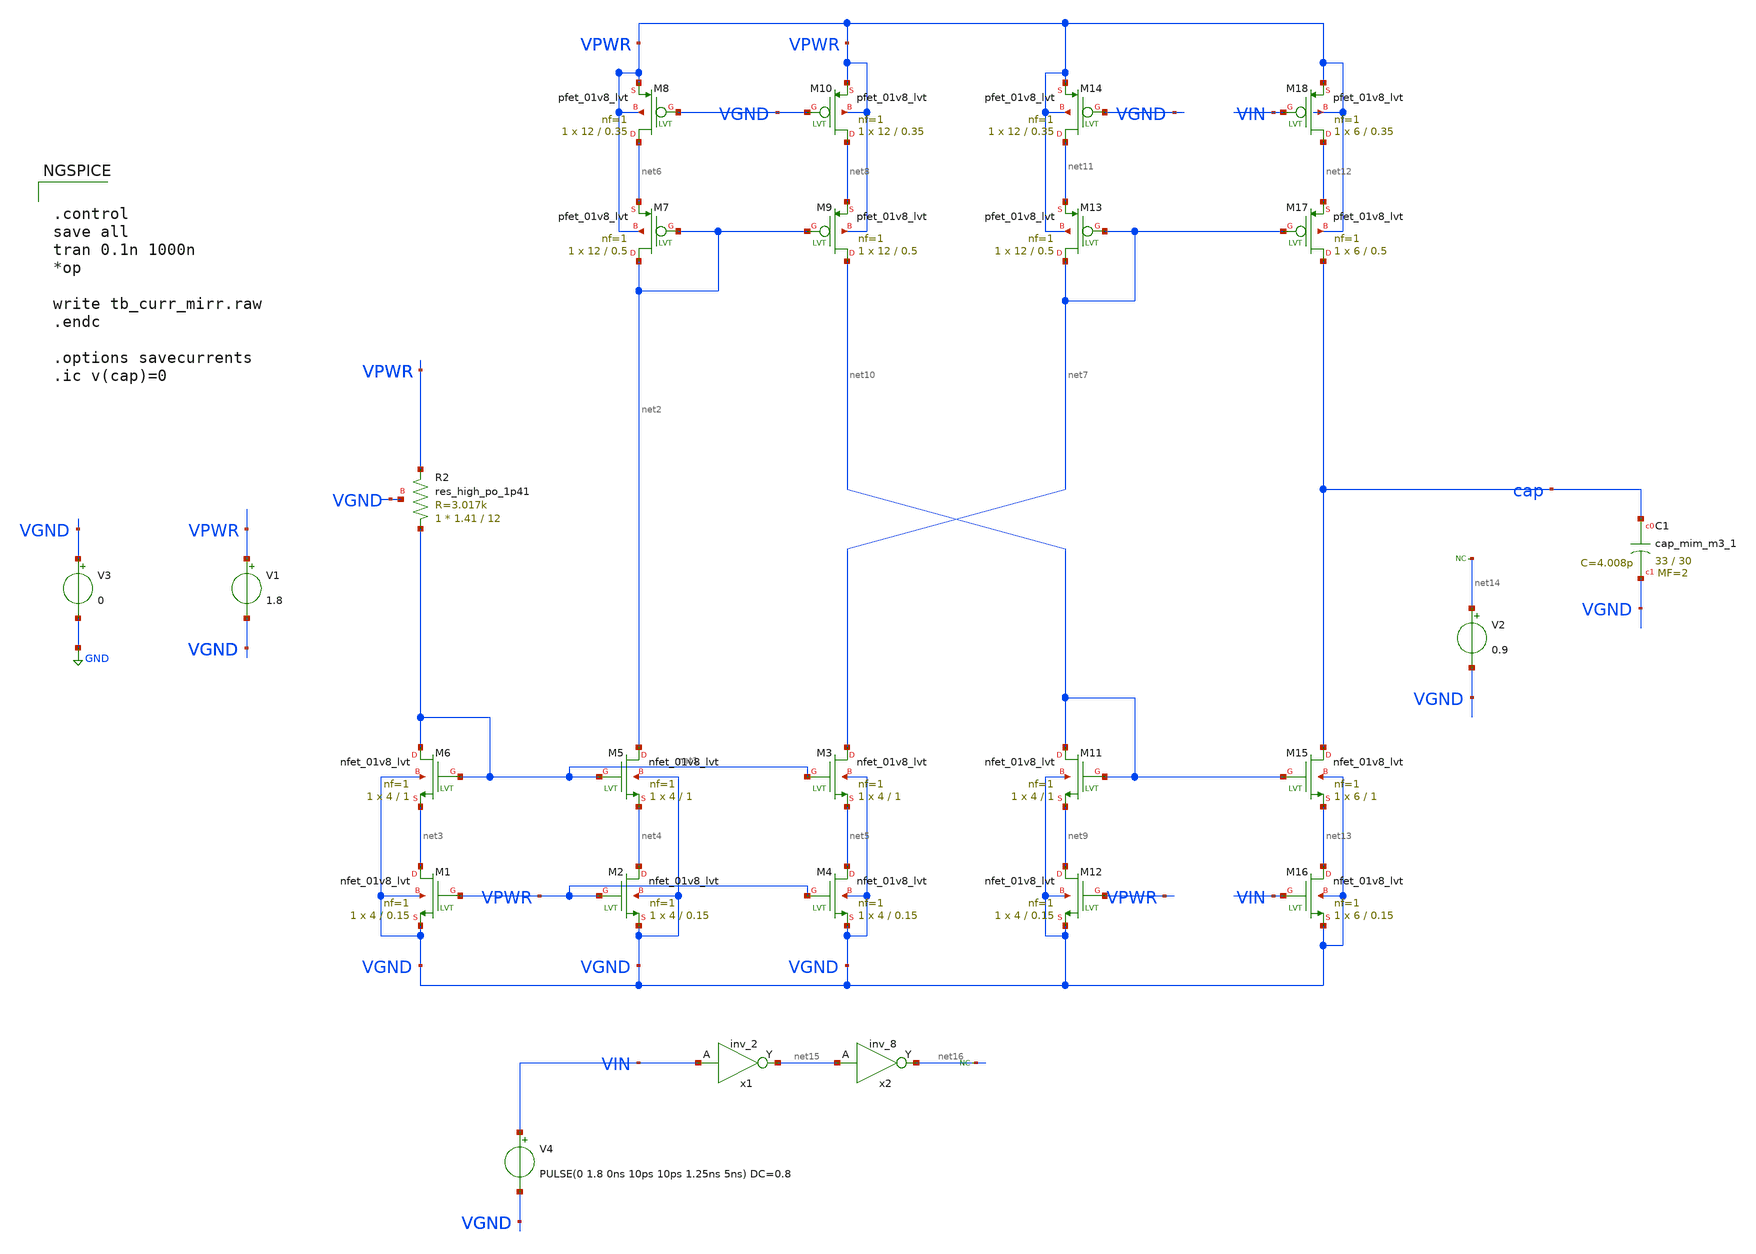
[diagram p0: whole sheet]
** sch_path: design/tb_curr_mirr.sch
**.subckt tb_curr_mirr
V1 VPWR VGND 1.8
V3 VGND GND 0
XM5 net2 net1 net4 VGND sky130_fd_pr__nfet_01v8_lvt L=1 W=4 nf=1 ad='int((nf+1)/2) * W/nf * 0.29' as='int((nf+2)/2) * W/nf * 0.29'
+ pd='2*int((nf+1)/2) * (W/nf + 0.29)' ps='2*int((nf+2)/2) * (W/nf + 0.29)' nrd='0.29 / W' nrs='0.29 / W'
+ sa=0 sb=0 sd=0 mult=1 m=1
XM6 net1 net1 net3 VGND sky130_fd_pr__nfet_01v8_lvt L=1 W=4 nf=1 ad='int((nf+1)/2) * W/nf * 0.29' as='int((nf+2)/2) * W/nf * 0.29'
+ pd='2*int((nf+1)/2) * (W/nf + 0.29)' ps='2*int((nf+2)/2) * (W/nf + 0.29)' nrd='0.29 / W' nrs='0.29 / W'
+ sa=0 sb=0 sd=0 mult=1 m=1
XM1 net3 VPWR VGND VGND sky130_fd_pr__nfet_01v8_lvt L=0.15 W=4 nf=1 ad='int((nf+1)/2) * W/nf * 0.29'
+ as='int((nf+2)/2) * W/nf * 0.29' pd='2*int((nf+1)/2) * (W/nf + 0.29)' ps='2*int((nf+2)/2) * (W/nf + 0.29)'
+ nrd='0.29 / W' nrs='0.29 / W' sa=0 sb=0 sd=0 mult=1 m=1
XM2 net4 VPWR VGND VGND sky130_fd_pr__nfet_01v8_lvt L=0.15 W=4 nf=1 ad='int((nf+1)/2) * W/nf * 0.29'
+ as='int((nf+2)/2) * W/nf * 0.29' pd='2*int((nf+1)/2) * (W/nf + 0.29)' ps='2*int((nf+2)/2) * (W/nf + 0.29)'
+ nrd='0.29 / W' nrs='0.29 / W' sa=0 sb=0 sd=0 mult=1 m=1
XM3 net7 net1 net5 VGND sky130_fd_pr__nfet_01v8_lvt L=1 W=4 nf=1 ad='int((nf+1)/2) * W/nf * 0.29' as='int((nf+2)/2) * W/nf * 0.29'
+ pd='2*int((nf+1)/2) * (W/nf + 0.29)' ps='2*int((nf+2)/2) * (W/nf + 0.29)' nrd='0.29 / W' nrs='0.29 / W'
+ sa=0 sb=0 sd=0 mult=1 m=1
XM4 net5 VPWR VGND VGND sky130_fd_pr__nfet_01v8_lvt L=0.15 W=4 nf=1 ad='int((nf+1)/2) * W/nf * 0.29'
+ as='int((nf+2)/2) * W/nf * 0.29' pd='2*int((nf+1)/2) * (W/nf + 0.29)' ps='2*int((nf+2)/2) * (W/nf + 0.29)'
+ nrd='0.29 / W' nrs='0.29 / W' sa=0 sb=0 sd=0 mult=1 m=1
XM7 net2 net2 net6 VPWR sky130_fd_pr__pfet_01v8_lvt L=0.5 W=12 nf=1 ad='int((nf+1)/2) * W/nf * 0.29'
+ as='int((nf+2)/2) * W/nf * 0.29' pd='2*int((nf+1)/2) * (W/nf + 0.29)' ps='2*int((nf+2)/2) * (W/nf + 0.29)'
+ nrd='0.29 / W' nrs='0.29 / W' sa=0 sb=0 sd=0 mult=1 m=1
XM8 net6 VGND VPWR VPWR sky130_fd_pr__pfet_01v8_lvt L=0.35 W=12 nf=1 ad='int((nf+1)/2) * W/nf * 0.29'
+ as='int((nf+2)/2) * W/nf * 0.29' pd='2*int((nf+1)/2) * (W/nf + 0.29)' ps='2*int((nf+2)/2) * (W/nf + 0.29)'
+ nrd='0.29 / W' nrs='0.29 / W' sa=0 sb=0 sd=0 mult=1 m=1
XM9 net10 net2 net8 VPWR sky130_fd_pr__pfet_01v8_lvt L=0.5 W=12 nf=1 ad='int((nf+1)/2) * W/nf * 0.29'
+ as='int((nf+2)/2) * W/nf * 0.29' pd='2*int((nf+1)/2) * (W/nf + 0.29)' ps='2*int((nf+2)/2) * (W/nf + 0.29)'
+ nrd='0.29 / W' nrs='0.29 / W' sa=0 sb=0 sd=0 mult=1 m=1
XM10 net8 VGND VPWR VPWR sky130_fd_pr__pfet_01v8_lvt L=0.35 W=12 nf=1 ad='int((nf+1)/2) * W/nf * 0.29'
+ as='int((nf+2)/2) * W/nf * 0.29' pd='2*int((nf+1)/2) * (W/nf + 0.29)' ps='2*int((nf+2)/2) * (W/nf + 0.29)'
+ nrd='0.29 / W' nrs='0.29 / W' sa=0 sb=0 sd=0 mult=1 m=1
XM11 net10 net10 net9 VGND sky130_fd_pr__nfet_01v8_lvt L=1 W=4 nf=1 ad='int((nf+1)/2) * W/nf * 0.29'
+ as='int((nf+2)/2) * W/nf * 0.29' pd='2*int((nf+1)/2) * (W/nf + 0.29)' ps='2*int((nf+2)/2) * (W/nf + 0.29)'
+ nrd='0.29 / W' nrs='0.29 / W' sa=0 sb=0 sd=0 mult=1 m=1
XM12 net9 VPWR VGND VGND sky130_fd_pr__nfet_01v8_lvt L=0.15 W=4 nf=1 ad='int((nf+1)/2) * W/nf * 0.29'
+ as='int((nf+2)/2) * W/nf * 0.29' pd='2*int((nf+1)/2) * (W/nf + 0.29)' ps='2*int((nf+2)/2) * (W/nf + 0.29)'
+ nrd='0.29 / W' nrs='0.29 / W' sa=0 sb=0 sd=0 mult=1 m=1
XM13 net7 net7 net11 VPWR sky130_fd_pr__pfet_01v8_lvt L=0.5 W=12 nf=1 ad='int((nf+1)/2) * W/nf * 0.29'
+ as='int((nf+2)/2) * W/nf * 0.29' pd='2*int((nf+1)/2) * (W/nf + 0.29)' ps='2*int((nf+2)/2) * (W/nf + 0.29)'
+ nrd='0.29 / W' nrs='0.29 / W' sa=0 sb=0 sd=0 mult=1 m=1
XM14 net11 VGND VPWR VPWR sky130_fd_pr__pfet_01v8_lvt L=0.35 W=12 nf=1 ad='int((nf+1)/2) * W/nf * 0.29'
+ as='int((nf+2)/2) * W/nf * 0.29' pd='2*int((nf+1)/2) * (W/nf + 0.29)' ps='2*int((nf+2)/2) * (W/nf + 0.29)'
+ nrd='0.29 / W' nrs='0.29 / W' sa=0 sb=0 sd=0 mult=1 m=1
XM15 cap net10 net13 VGND sky130_fd_pr__nfet_01v8_lvt L=1 W=6 nf=1 ad='int((nf+1)/2) * W/nf * 0.29' as='int((nf+2)/2) * W/nf * 0.29'
+ pd='2*int((nf+1)/2) * (W/nf + 0.29)' ps='2*int((nf+2)/2) * (W/nf + 0.29)' nrd='0.29 / W' nrs='0.29 / W'
+ sa=0 sb=0 sd=0 mult=1 m=1
XM17 cap net7 net12 VPWR sky130_fd_pr__pfet_01v8_lvt L=0.5 W=6 nf=1 ad='int((nf+1)/2) * W/nf * 0.29'
+ as='int((nf+2)/2) * W/nf * 0.29' pd='2*int((nf+1)/2) * (W/nf + 0.29)' ps='2*int((nf+2)/2) * (W/nf + 0.29)'
+ nrd='0.29 / W' nrs='0.29 / W' sa=0 sb=0 sd=0 mult=1 m=1
XM18 net12 VIN VPWR VPWR sky130_fd_pr__pfet_01v8_lvt L=0.35 W=6 nf=1 ad='int((nf+1)/2) * W/nf * 0.29'
+ as='int((nf+2)/2) * W/nf * 0.29' pd='2*int((nf+1)/2) * (W/nf + 0.29)' ps='2*int((nf+2)/2) * (W/nf + 0.29)'
+ nrd='0.29 / W' nrs='0.29 / W' sa=0 sb=0 sd=0 mult=1 m=1
V2 net14 VGND 0.9
V4 VIN VGND PULSE(0 1.8 0ns 10ps 10ps 1.25ns 5ns) DC=0.8
XM16 net13 VIN VGND VGND sky130_fd_pr__nfet_01v8_lvt L=0.15 W=6 nf=1 ad='int((nf+1)/2) * W/nf * 0.29'
+ as='int((nf+2)/2) * W/nf * 0.29' pd='2*int((nf+1)/2) * (W/nf + 0.29)' ps='2*int((nf+2)/2) * (W/nf + 0.29)'
+ nrd='0.29 / W' nrs='0.29 / W' sa=0 sb=0 sd=0 mult=1 m=1
XC1 cap VGND sky130_fd_pr__cap_mim_m3_1 W=33 L=30 MF=2 m=2
XR2 net1 VPWR VGND sky130_fd_pr__res_high_po_1p41 L=12 mult=1 m=1
* noconn #net14
x1 VIN VGND VGND VPWR VPWR net15 sky130_fd_sc_hd__inv_2
x2 net15 VGND VGND VPWR VPWR net16 sky130_fd_sc_hd__inv_8
* noconn #net16
**** begin user architecture code

** opencircuitdesign pdks install
.lib $::SKYWATER_MODELS/sky130.lib.spice tt
.include $::SKYWATER_STDCELLS/sky130_fd_sc_hd.spice




.control
save all
tran 0.1n 1000n
*op

write tb_curr_mirr.raw
.endc

.options savecurrents
.ic v(cap)=0


**** end user architecture code
**.ends
.GLOBAL GND
.end
